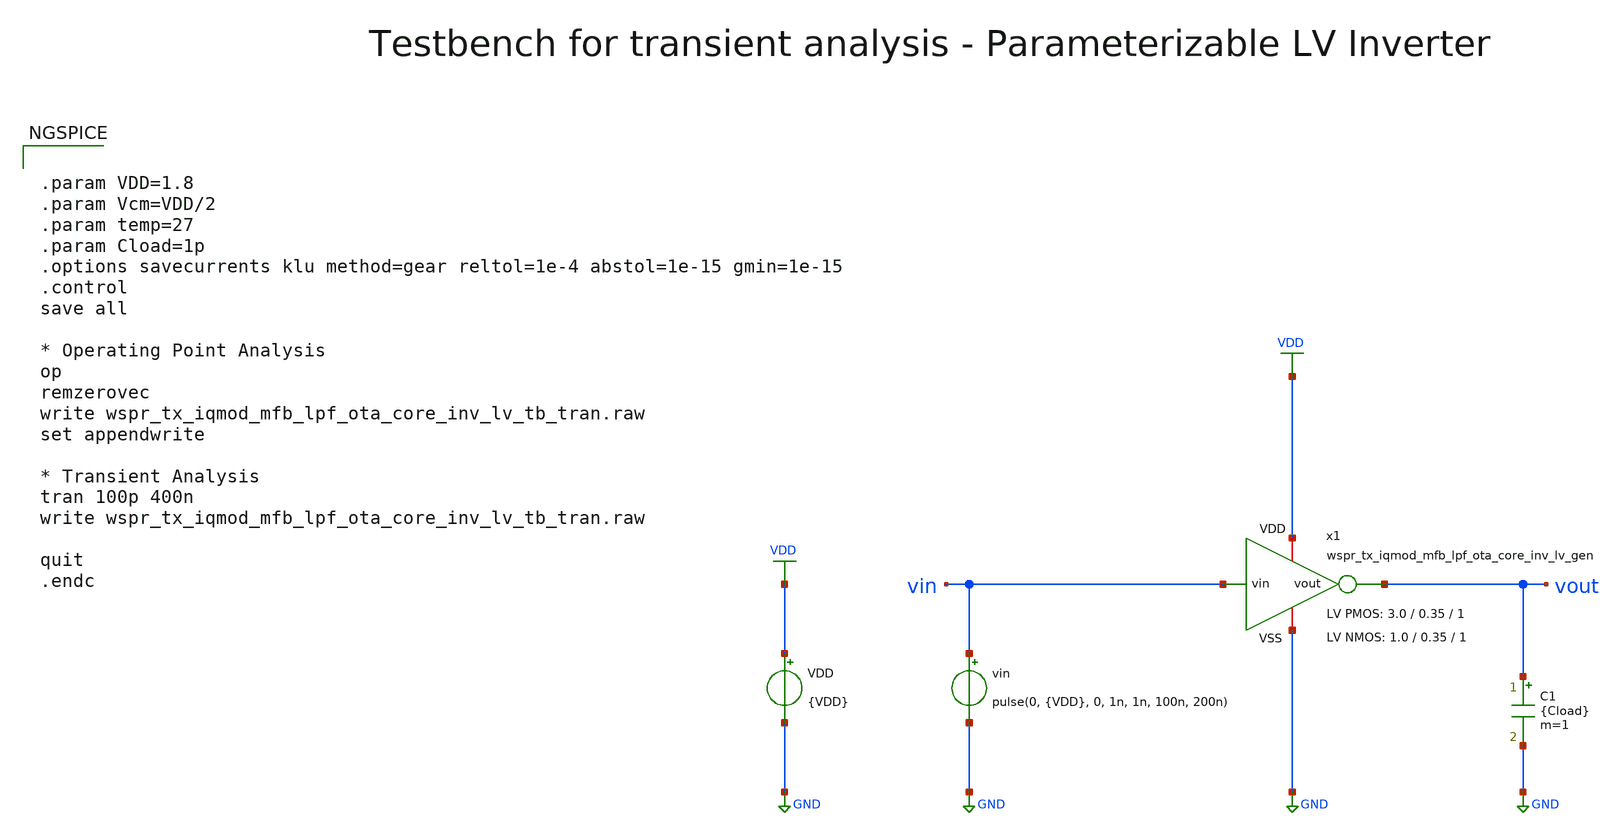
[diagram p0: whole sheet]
** sch_path: sky130/macros/iqmod/testbenches/wspr_tx_iqmod_mfb_lpf_ota_core_inv_lv_tb_tran.sch
**.subckt wspr_tx_iqmod_mfb_lpf_ota_core_inv_lv_tb_tran
VDD VDD GND {VDD}
vin vin GND pulse(0, {VDD}, 0, 1n, 1n, 100n, 200n)
C1 vout GND {Cload} m=1
x1 VDD vin vout GND wspr_tx_iqmod_mfb_lpf_ota_core_inv_lv_gen W_P=3.0 L_P=0.35 NF_P=1 W_N=1.0
+ L_N=0.35 NF_N=1
**** begin user architecture code


.param VDD=1.8
.param Vcm=VDD/2
.param temp=27
.param Cload=1p
.options savecurrents klu method=gear reltol=1e-4 abstol=1e-15 gmin=1e-15
.control
save all

* Operating Point Analysis
op
remzerovec
write wspr_tx_iqmod_mfb_lpf_ota_core_inv_lv_tb_tran.raw
set appendwrite

* Transient Analysis
tran 100p 400n
write wspr_tx_iqmod_mfb_lpf_ota_core_inv_lv_tb_tran.raw

quit
.endc


.lib $::SKYWATER_MODELS/sky130.lib.spice tt
**** end user architecture code
**.ends
.GLOBAL GND
.GLOBAL VDD
.end
